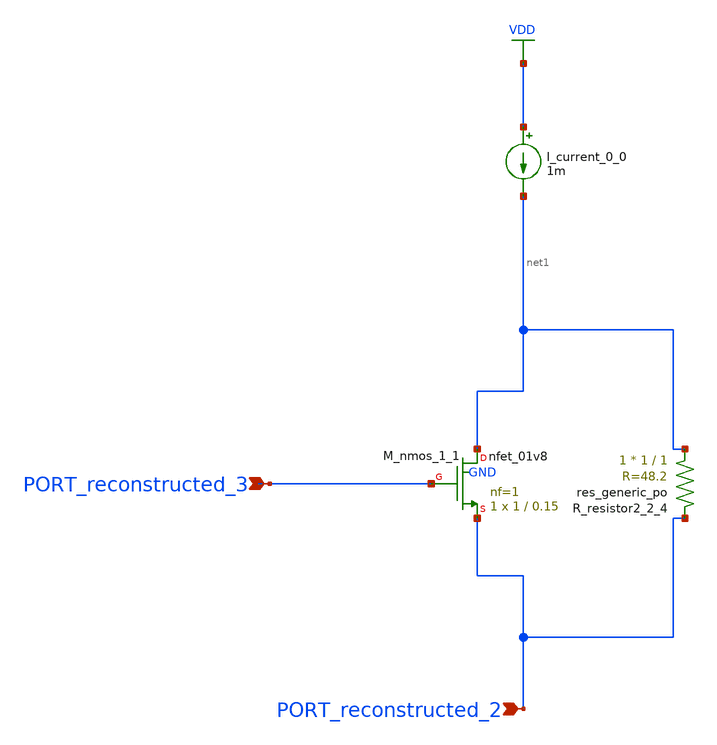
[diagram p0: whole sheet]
** sch_path: schematics/AMSNet/357.sch
**.subckt 357 PORT_reconstructed_3 PORT_reconstructed_2
*.ipin PORT_reconstructed_3
*.ipin PORT_reconstructed_2
I_current_0_0 VDD net1 1m
XM_nmos_1_1 net1 PORT_reconstructed_3 PORT_reconstructed_2 GND sky130_fd_pr__nfet_01v8 L=0.15 W=1 nf=1
+ ad='int((1 + 1)/2) * 1 / 1 * 0.29' as='int((1 + 2)/2) * 1 / 1 * 0.29' pd='2*int((1 + 1)/2) * (1 / 1 + 0.29)'
+ ps='2*int((1 + 2)/2) * (1 / 1 + 0.29)' nrd='0.29 / 1 ' nrs='0.29 / 1 ' sa=0 sb=0 sd=0 mult=1 m=1
XR_resistor2_2_4 net1 PORT_reconstructed_2 sky130_fd_pr__res_generic_po W=1 L=1 m=1
**.ends
.GLOBAL VDD
.end
